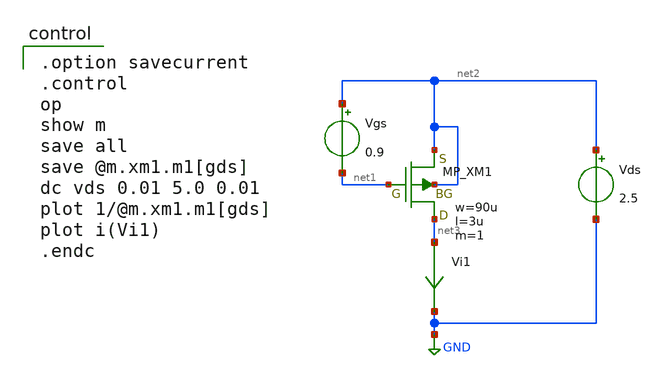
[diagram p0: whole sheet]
** sch_path: member_project/OPAMP/ShuntaroOhno/xschem/ibias_rds.sch
**.subckt ibias_rds
Vgs net2 net1 0.9
Vds net2 GND 2.5
XM1 net3 net1 net2 net2 PMOS w=90u l=3u as=0 ad=0 ps=0 pd=0 nrd=0 nrs=0 m=1
Vi1 net3 GND 0
.save i(vi1)
**** begin user architecture code

.option savecurrent
.control
op
show m
save all
save @m.xm1.m1[gds]
dc vds 0.01 5.0 0.01
plot 1/@m.xm1.m1[gds]
plot i(Vi1)
.endc

 .include $::LIB/../ip62_models
**** end user architecture code
**.ends
.GLOBAL GND
.end
